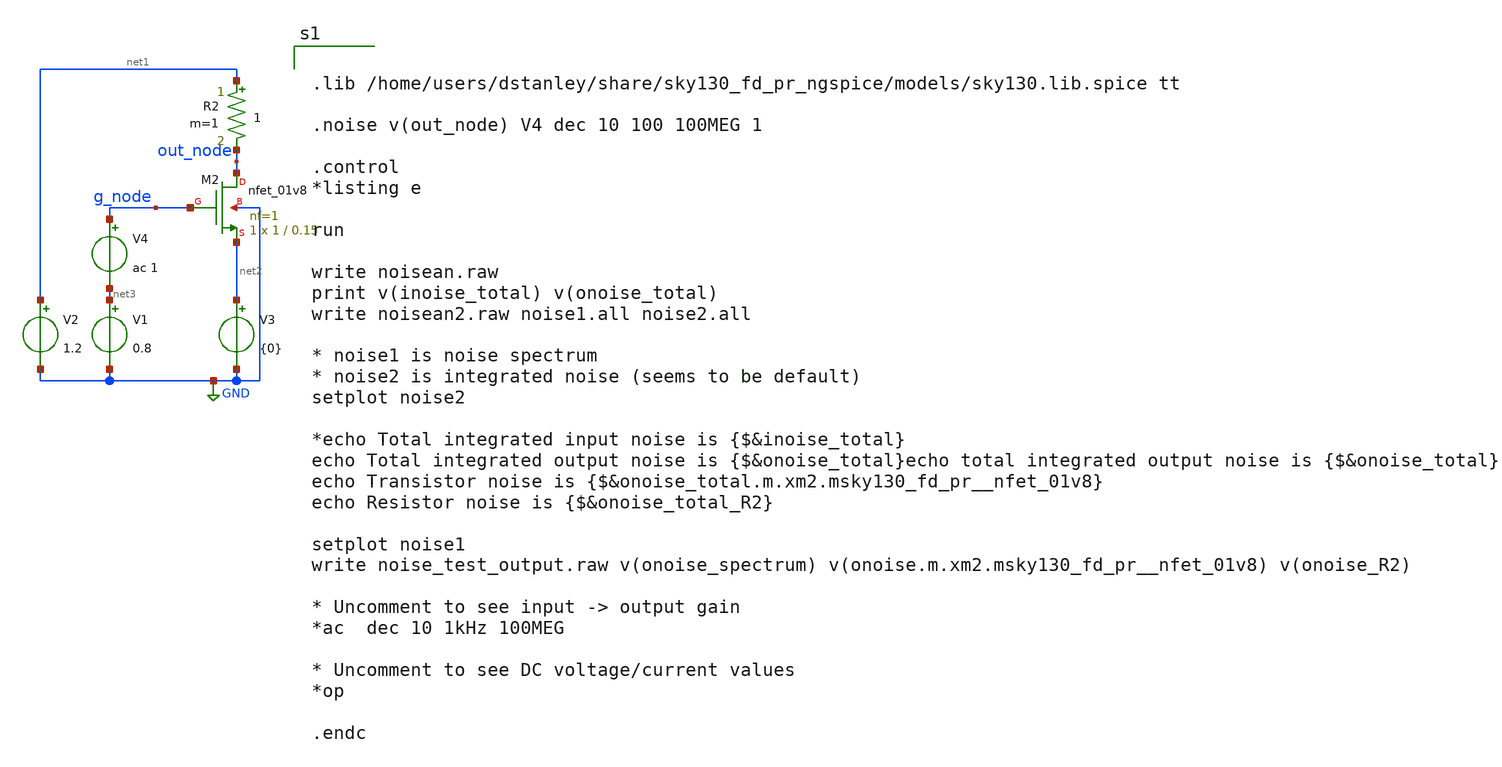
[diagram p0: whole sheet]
** sch_path: noise_test2.sch
**.subckt noise_test2
V1 net3 GND 0.8
V2 net1 GND 1.2
XM2 out_node g_node net2 GND sky130_fd_pr__nfet_01v8 L=0.15 W=1 nf=1 ad='int((nf+1)/2) * W/nf * 0.29'
+ as='int((nf+2)/2) * W/nf * 0.29' pd='2*int((nf+1)/2) * (W/nf + 0.29)' ps='2*int((nf+2)/2) * (W/nf + 0.29)'
+ nrd='0.29 / W' nrs='0.29 / W' sa=0 sb=0 sd=0 mult=1 m=1
V3 net2 GND {0}
V4 g_node net3 ac 1
R2 net1 out_node 1 m=1
**** begin user architecture code


.lib /home/users/dstanley/share/sky130_fd_pr_ngspice/models/sky130.lib.spice tt

.noise v(out_node) V4 dec 10 100 100MEG 1

.control
*listing e

run

write noisean.raw
print v(inoise_total) v(onoise_total)
write noisean2.raw noise1.all noise2.all

* noise1 is noise spectrum
* noise2 is integrated noise (seems to be default)
setplot noise2

*echo Total integrated input noise is {$&inoise_total}
echo Total integrated output noise is {$&onoise_total}echo total integrated output noise is {$&onoise_total}
echo Transistor noise is {$&onoise_total.m.xm2.msky130_fd_pr__nfet_01v8}
echo Resistor noise is {$&onoise_total_R2}

setplot noise1
write noise_test_output.raw v(onoise_spectrum) v(onoise.m.xm2.msky130_fd_pr__nfet_01v8) v(onoise_R2)

* Uncomment to see input -> output gain
*ac  dec 10 1kHz 100MEG

* Uncomment to see DC voltage/current values
*op

.endc


**** end user architecture code
**.ends
.GLOBAL GND
.end
